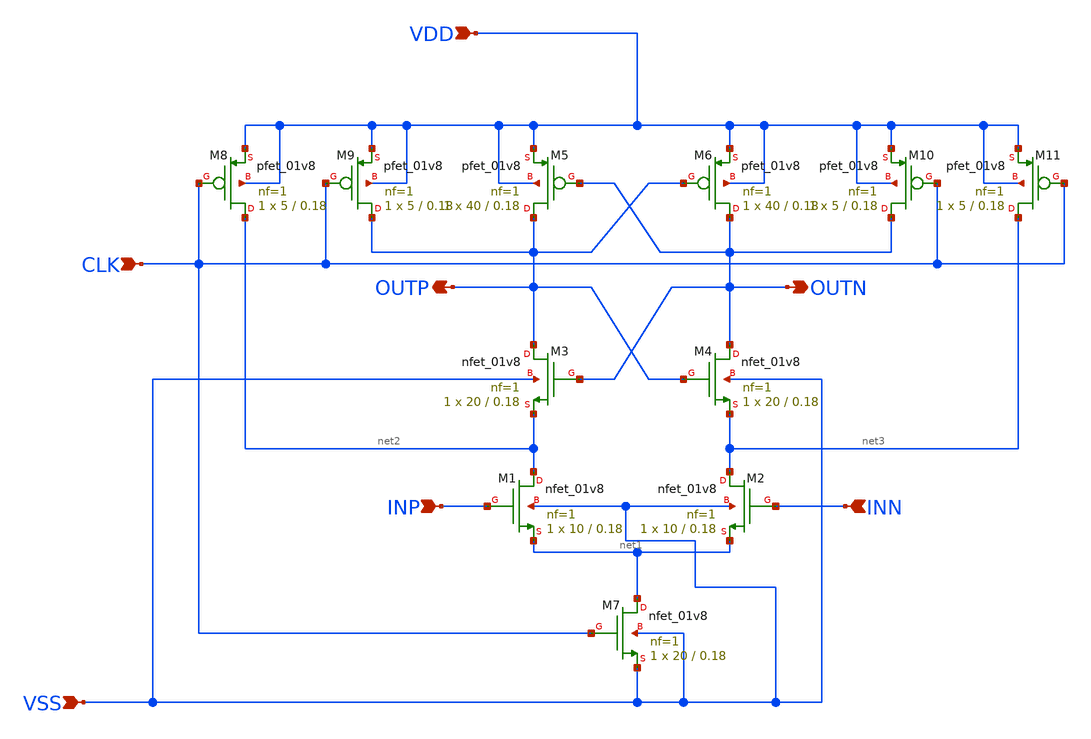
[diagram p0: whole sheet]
** sch_path: design/ADI_SA_SKY130A/ADI_SA.sch
**.subckt ADI_SA VDD VSS OUTP OUTN CLK INP INN
*.ipin VDD
*.ipin VSS
*.opin OUTP
*.opin OUTN
*.ipin CLK
*.ipin INP
*.ipin INN
XM1 net2 INP net1 VSS sky130_fd_pr__nfet_01v8 L=0.18 W=10 nf=1 ad='int((nf+1)/2) * W/nf * 0.29' as='int((nf+2)/2) * W/nf * 0.29'
+ pd='2*int((nf+1)/2) * (W/nf + 0.29)' ps='2*int((nf+2)/2) * (W/nf + 0.29)' nrd='0.29 / W' nrs='0.29 / W'
+ sa=0 sb=0 sd=0 mult=1 m=1
XM2 net3 INN net1 VSS sky130_fd_pr__nfet_01v8 L=0.18 W=10 nf=1 ad='int((nf+1)/2) * W/nf * 0.29' as='int((nf+2)/2) * W/nf * 0.29'
+ pd='2*int((nf+1)/2) * (W/nf + 0.29)' ps='2*int((nf+2)/2) * (W/nf + 0.29)' nrd='0.29 / W' nrs='0.29 / W'
+ sa=0 sb=0 sd=0 mult=1 m=1
XM3 OUTP OUTN net2 VSS sky130_fd_pr__nfet_01v8 L=0.18 W=20 nf=1 ad='int((nf+1)/2) * W/nf * 0.29' as='int((nf+2)/2) * W/nf * 0.29'
+ pd='2*int((nf+1)/2) * (W/nf + 0.29)' ps='2*int((nf+2)/2) * (W/nf + 0.29)' nrd='0.29 / W' nrs='0.29 / W'
+ sa=0 sb=0 sd=0 mult=1 m=1
XM4 OUTN OUTP net3 VSS sky130_fd_pr__nfet_01v8 L=0.18 W=20 nf=1 ad='int((nf+1)/2) * W/nf * 0.29' as='int((nf+2)/2) * W/nf * 0.29'
+ pd='2*int((nf+1)/2) * (W/nf + 0.29)' ps='2*int((nf+2)/2) * (W/nf + 0.29)' nrd='0.29 / W' nrs='0.29 / W'
+ sa=0 sb=0 sd=0 mult=1 m=1
XM5 OUTP OUTN VDD VDD sky130_fd_pr__pfet_01v8 L=0.18 W=40 nf=1 ad='int((nf+1)/2) * W/nf * 0.29' as='int((nf+2)/2) * W/nf * 0.29'
+ pd='2*int((nf+1)/2) * (W/nf + 0.29)' ps='2*int((nf+2)/2) * (W/nf + 0.29)' nrd='0.29 / W' nrs='0.29 / W'
+ sa=0 sb=0 sd=0 mult=1 m=1
XM6 OUTN OUTP VDD VDD sky130_fd_pr__pfet_01v8 L=0.18 W=40 nf=1 ad='int((nf+1)/2) * W/nf * 0.29' as='int((nf+2)/2) * W/nf * 0.29'
+ pd='2*int((nf+1)/2) * (W/nf + 0.29)' ps='2*int((nf+2)/2) * (W/nf + 0.29)' nrd='0.29 / W' nrs='0.29 / W'
+ sa=0 sb=0 sd=0 mult=1 m=1
XM7 net1 CLK VSS VSS sky130_fd_pr__nfet_01v8 L=0.18 W=20 nf=1 ad='int((nf+1)/2) * W/nf * 0.29' as='int((nf+2)/2) * W/nf * 0.29'
+ pd='2*int((nf+1)/2) * (W/nf + 0.29)' ps='2*int((nf+2)/2) * (W/nf + 0.29)' nrd='0.29 / W' nrs='0.29 / W'
+ sa=0 sb=0 sd=0 mult=1 m=1
XM8 net2 CLK VDD VDD sky130_fd_pr__pfet_01v8 L=0.18 W=5 nf=1 ad='int((nf+1)/2) * W/nf * 0.29' as='int((nf+2)/2) * W/nf * 0.29'
+ pd='2*int((nf+1)/2) * (W/nf + 0.29)' ps='2*int((nf+2)/2) * (W/nf + 0.29)' nrd='0.29 / W' nrs='0.29 / W'
+ sa=0 sb=0 sd=0 mult=1 m=1
XM9 OUTP CLK VDD VDD sky130_fd_pr__pfet_01v8 L=0.18 W=5 nf=1 ad='int((nf+1)/2) * W/nf * 0.29' as='int((nf+2)/2) * W/nf * 0.29'
+ pd='2*int((nf+1)/2) * (W/nf + 0.29)' ps='2*int((nf+2)/2) * (W/nf + 0.29)' nrd='0.29 / W' nrs='0.29 / W'
+ sa=0 sb=0 sd=0 mult=1 m=1
XM10 OUTN CLK VDD VDD sky130_fd_pr__pfet_01v8 L=0.18 W=5 nf=1 ad='int((nf+1)/2) * W/nf * 0.29' as='int((nf+2)/2) * W/nf * 0.29'
+ pd='2*int((nf+1)/2) * (W/nf + 0.29)' ps='2*int((nf+2)/2) * (W/nf + 0.29)' nrd='0.29 / W' nrs='0.29 / W'
+ sa=0 sb=0 sd=0 mult=1 m=1
XM11 net3 CLK VDD VDD sky130_fd_pr__pfet_01v8 L=0.18 W=5 nf=1 ad='int((nf+1)/2) * W/nf * 0.29' as='int((nf+2)/2) * W/nf * 0.29'
+ pd='2*int((nf+1)/2) * (W/nf + 0.29)' ps='2*int((nf+2)/2) * (W/nf + 0.29)' nrd='0.29 / W' nrs='0.29 / W'
+ sa=0 sb=0 sd=0 mult=1 m=1
**.ends
.end
